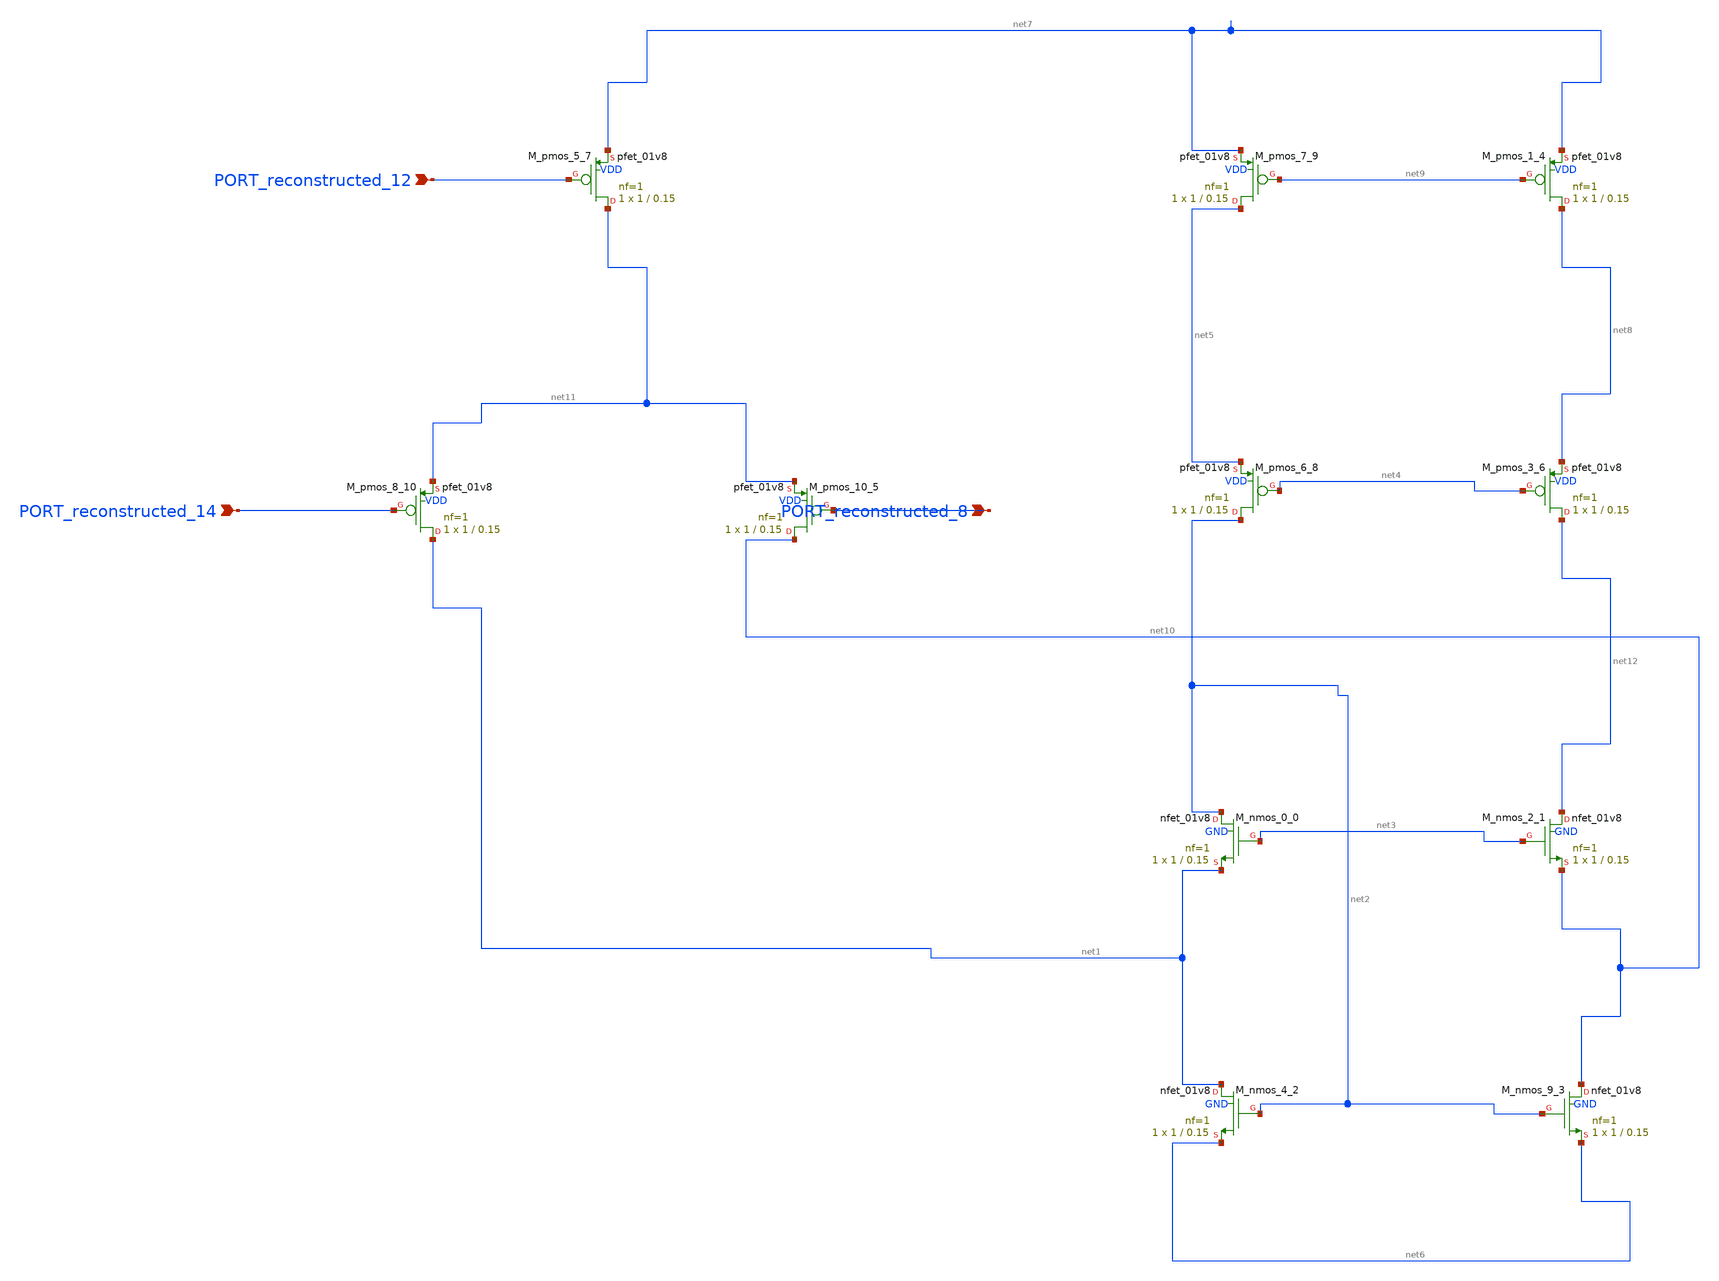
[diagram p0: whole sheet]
** sch_path: schematics/p02_fig1_input_stage.sch
**.subckt p02_fig1_input_stage PORT_reconstructed_14 PORT_reconstructed_8 PORT_reconstructed_12
*.ipin PORT_reconstructed_14
*.ipin PORT_reconstructed_8
*.ipin PORT_reconstructed_12
XM_nmos_0_0 net2 net3 net1 GND sky130_fd_pr__nfet_01v8 L=0.15 W=1 nf=1 ad='int((1 + 1)/2) * 1 / 1 * 0.29'
+ as='int((1 + 2)/2) * 1 / 1 * 0.29' pd='2*int((1 + 1)/2) * (1 / 1 + 0.29)' ps='2*int((1 + 2)/2) * (1 / 1 + 0.29)'
+ nrd='0.29 / 1 ' nrs='0.29 / 1 ' sa=0 sb=0 sd=0 mult=1 m=1
XM_nmos_2_1 net12 net3 net10 GND sky130_fd_pr__nfet_01v8 L=0.15 W=1 nf=1 ad='int((1 + 1)/2) * 1 / 1 * 0.29'
+ as='int((1 + 2)/2) * 1 / 1 * 0.29' pd='2*int((1 + 1)/2) * (1 / 1 + 0.29)' ps='2*int((1 + 2)/2) * (1 / 1 + 0.29)'
+ nrd='0.29 / 1 ' nrs='0.29 / 1 ' sa=0 sb=0 sd=0 mult=1 m=1
XM_nmos_4_2 net1 net2 net6 GND sky130_fd_pr__nfet_01v8 L=0.15 W=1 nf=1 ad='int((1 + 1)/2) * 1 / 1 * 0.29'
+ as='int((1 + 2)/2) * 1 / 1 * 0.29' pd='2*int((1 + 1)/2) * (1 / 1 + 0.29)' ps='2*int((1 + 2)/2) * (1 / 1 + 0.29)'
+ nrd='0.29 / 1 ' nrs='0.29 / 1 ' sa=0 sb=0 sd=0 mult=1 m=1
XM_nmos_9_3 net10 net2 net6 GND sky130_fd_pr__nfet_01v8 L=0.15 W=1 nf=1 ad='int((1 + 1)/2) * 1 / 1 * 0.29'
+ as='int((1 + 2)/2) * 1 / 1 * 0.29' pd='2*int((1 + 1)/2) * (1 / 1 + 0.29)' ps='2*int((1 + 2)/2) * (1 / 1 + 0.29)'
+ nrd='0.29 / 1 ' nrs='0.29 / 1 ' sa=0 sb=0 sd=0 mult=1 m=1
XM_pmos_1_4 net8 net9 net7 VDD sky130_fd_pr__pfet_01v8 L=0.15 W=1 nf=1 ad='int((1 + 1)/2) * 1 / 1 * 0.29'
+ as='int((1 + 2)/2) * 1 / 1 * 0.29' pd='2*int((1 + 1)/2) * (1 / 1 + 0.29)' ps='2*int((1 + 2)/2) * (1 / 1 + 0.29)'
+ nrd='0.29 / 1 ' nrs='0.29 / 1 ' sa=0 sb=0 sd=0 mult=1 m=1
XM_pmos_10_5 net10 PORT_reconstructed_8 net11 VDD sky130_fd_pr__pfet_01v8 L=0.15 W=1 nf=1 ad='int((1 + 1)/2) * 1 / 1 * 0.29'
+ as='int((1 + 2)/2) * 1 / 1 * 0.29' pd='2*int((1 + 1)/2) * (1 / 1 + 0.29)' ps='2*int((1 + 2)/2) * (1 / 1 + 0.29)'
+ nrd='0.29 / 1 ' nrs='0.29 / 1 ' sa=0 sb=0 sd=0 mult=1 m=1
XM_pmos_3_6 net12 net4 net8 VDD sky130_fd_pr__pfet_01v8 L=0.15 W=1 nf=1 ad='int((1 + 1)/2) * 1 / 1 * 0.29'
+ as='int((1 + 2)/2) * 1 / 1 * 0.29' pd='2*int((1 + 1)/2) * (1 / 1 + 0.29)' ps='2*int((1 + 2)/2) * (1 / 1 + 0.29)'
+ nrd='0.29 / 1 ' nrs='0.29 / 1 ' sa=0 sb=0 sd=0 mult=1 m=1
XM_pmos_5_7 net11 PORT_reconstructed_12 net7 VDD sky130_fd_pr__pfet_01v8 L=0.15 W=1 nf=1 ad='int((1 + 1)/2) * 1 / 1 * 0.29'
+ as='int((1 + 2)/2) * 1 / 1 * 0.29' pd='2*int((1 + 1)/2) * (1 / 1 + 0.29)' ps='2*int((1 + 2)/2) * (1 / 1 + 0.29)'
+ nrd='0.29 / 1 ' nrs='0.29 / 1 ' sa=0 sb=0 sd=0 mult=1 m=1
XM_pmos_6_8 net2 net4 net5 VDD sky130_fd_pr__pfet_01v8 L=0.15 W=1 nf=1 ad='int((1 + 1)/2) * 1 / 1 * 0.29'
+ as='int((1 + 2)/2) * 1 / 1 * 0.29' pd='2*int((1 + 1)/2) * (1 / 1 + 0.29)' ps='2*int((1 + 2)/2) * (1 / 1 + 0.29)'
+ nrd='0.29 / 1 ' nrs='0.29 / 1 ' sa=0 sb=0 sd=0 mult=1 m=1
XM_pmos_7_9 net5 net9 net7 VDD sky130_fd_pr__pfet_01v8 L=0.15 W=1 nf=1 ad='int((1 + 1)/2) * 1 / 1 * 0.29'
+ as='int((1 + 2)/2) * 1 / 1 * 0.29' pd='2*int((1 + 1)/2) * (1 / 1 + 0.29)' ps='2*int((1 + 2)/2) * (1 / 1 + 0.29)'
+ nrd='0.29 / 1 ' nrs='0.29 / 1 ' sa=0 sb=0 sd=0 mult=1 m=1
XM_pmos_8_10 net1 PORT_reconstructed_14 net11 VDD sky130_fd_pr__pfet_01v8 L=0.15 W=1 nf=1 ad='int((1 + 1)/2) * 1 / 1 * 0.29'
+ as='int((1 + 2)/2) * 1 / 1 * 0.29' pd='2*int((1 + 1)/2) * (1 / 1 + 0.29)' ps='2*int((1 + 2)/2) * (1 / 1 + 0.29)'
+ nrd='0.29 / 1 ' nrs='0.29 / 1 ' sa=0 sb=0 sd=0 mult=1 m=1
**.ends
.end
